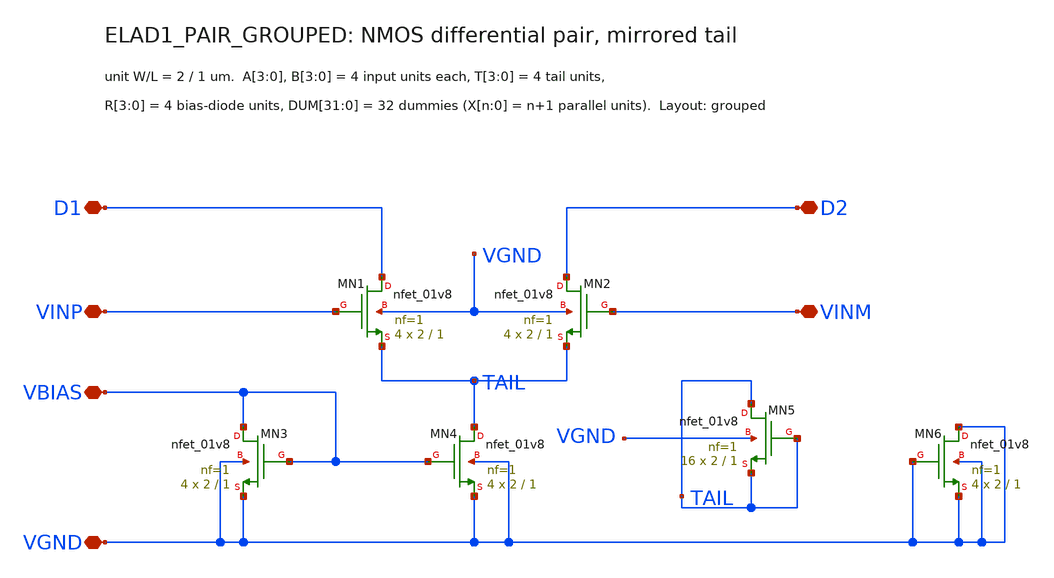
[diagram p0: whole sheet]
** sch_path: cells/ELAD1_PAIR_GROUPED/schematic/ELAD1_PAIR_GROUPED.sch
**.subckt ELAD1_PAIR_GROUPED D1 D2 VINP VINM VBIAS VGND
*.iopin D1
*.iopin D2
*.iopin VINP
*.iopin VINM
*.iopin VBIAS
*.iopin VGND
XMN1 D1 VINP TAIL VGND sky130_fd_pr__nfet_01v8 L=1 W=2 nf=1 ad='int((1 + 1)/2) * 2 / 1 * 0.29' as='int((1 + 2)/2) * 2 / 1 * 0.29'
+ pd='2*int((1 + 1)/2) * (2 / 1 + 0.29)' ps='2*int((1 + 2)/2) * (2 / 1 + 0.29)' nrd='0.29 / 2 ' nrs='0.29 / 2 '
+ sa=0 sb=0 sd=0 mult=4 m=4
XMN2 D2 VINM TAIL VGND sky130_fd_pr__nfet_01v8 L=1 W=2 nf=1 ad='int((1 + 1)/2) * 2 / 1 * 0.29' as='int((1 + 2)/2) * 2 / 1 * 0.29'
+ pd='2*int((1 + 1)/2) * (2 / 1 + 0.29)' ps='2*int((1 + 2)/2) * (2 / 1 + 0.29)' nrd='0.29 / 2 ' nrs='0.29 / 2 '
+ sa=0 sb=0 sd=0 mult=4 m=4
XMN4 TAIL VBIAS VGND VGND sky130_fd_pr__nfet_01v8 L=1 W=2 nf=1 ad='int((1 + 1)/2) * 2 / 1 * 0.29' as='int((1 + 2)/2) * 2 / 1 * 0.29'
+ pd='2*int((1 + 1)/2) * (2 / 1 + 0.29)' ps='2*int((1 + 2)/2) * (2 / 1 + 0.29)' nrd='0.29 / 2 ' nrs='0.29 / 2 '
+ sa=0 sb=0 sd=0 mult=4 m=4
XMN3 VBIAS VBIAS VGND VGND sky130_fd_pr__nfet_01v8 L=1 W=2 nf=1 ad='int((1 + 1)/2) * 2 / 1 * 0.29' as='int((1 + 2)/2) * 2 / 1 * 0.29'
+ pd='2*int((1 + 1)/2) * (2 / 1 + 0.29)' ps='2*int((1 + 2)/2) * (2 / 1 + 0.29)' nrd='0.29 / 2 ' nrs='0.29 / 2 '
+ sa=0 sb=0 sd=0 mult=4 m=4
XMN6 VGND VGND VGND VGND sky130_fd_pr__nfet_01v8 L=1 W=2 nf=1 ad='int((1 + 1)/2) * 2 / 1 * 0.29' as='int((1 + 2)/2) * 2 / 1 * 0.29'
+ pd='2*int((1 + 1)/2) * (2 / 1 + 0.29)' ps='2*int((1 + 2)/2) * (2 / 1 + 0.29)' nrd='0.29 / 2 ' nrs='0.29 / 2 '
+ sa=0 sb=0 sd=0 mult=4 m=4
XMN5 TAIL TAIL TAIL VGND sky130_fd_pr__nfet_01v8 L=1 W=2 nf=1 ad='int((1 + 1)/2) * 2 / 1 * 0.29' as='int((1 + 2)/2) * 2 / 1 * 0.29'
+ pd='2*int((1 + 1)/2) * (2 / 1 + 0.29)' ps='2*int((1 + 2)/2) * (2 / 1 + 0.29)' nrd='0.29 / 2 ' nrs='0.29 / 2 '
+ sa=0 sb=0 sd=0 mult=16 m=16
**.ends
.end
